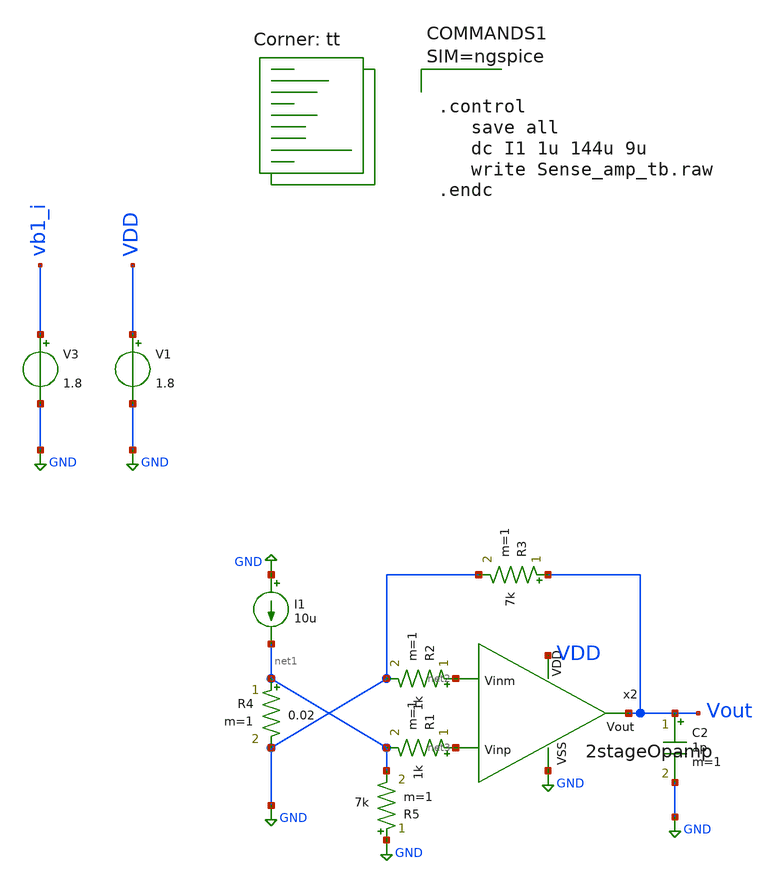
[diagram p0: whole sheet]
** sch_path: xschem/test/xschem/untitled-2.sch
**.subckt untitled-2
I1 GND net1 10u
V1 VDD GND 1.8
V3 vb1_i GND 1.8
x2 VDD net2 net3 Vout GND 2stageOpamp
R4 net1 GND 0.02 m=1
C2 Vout GND 1p m=1
R1 net3 net1 1k m=1
R2 net2 GND 1k m=1
R3 Vout GND 7k m=1
R5 GND net1 7k m=1
**** begin user architecture code
.lib $::SKYWATER_MODELS/sky130.lib.spice tt



.control
   save all
   dc I1 1u 144u 9u
   write Sense_amp_tb.raw
.endc



**** end user architecture code
**.ends

* expanding   symbol:  amplifiers/dec24/2stageOpamp.sym # of pins=5
** sym_path: amplifiers/dec24/2stageOpamp.sym
** sch_path: amplifiers/dec24/2stageOpamp.sch
.subckt 2stageOpamp VDD Vinm Vinp Vout VSS
*.ipin Vinm
*.ipin Vinp
*.opin Vout
*.ipin VSS
*.ipin VDD
XM8 Vout net1 VSS VSS sky130_fd_pr__nfet_01v8 L=1 W=6 nf=1 ad='int((nf+1)/2) * W/nf * 0.29' as='int((nf+2)/2) * W/nf * 0.29'
+ pd='2*int((nf+1)/2) * (W/nf + 0.29)' ps='2*int((nf+2)/2) * (W/nf + 0.29)' nrd='0.29 / W' nrs='0.29 / W'
+ sa=0 sb=0 sd=0 mult=8 m=8
XM2 Vout Vb1 VDD VDD sky130_fd_pr__pfet_01v8_lvt L=1 W=9 nf=1 ad='int((nf+1)/2) * W/nf * 0.29' as='int((nf+2)/2) * W/nf * 0.29'
+ pd='2*int((nf+1)/2) * (W/nf + 0.29)' ps='2*int((nf+2)/2) * (W/nf + 0.29)' nrd='0.29 / W' nrs='0.29 / W'
+ sa=0 sb=0 sd=0 mult=3 m=3
XM5 net5 Vb3 net6 VSS sky130_fd_pr__nfet_01v8 L=1 W=4 nf=1 ad='int((nf+1)/2) * W/nf * 0.29' as='int((nf+2)/2) * W/nf * 0.29'
+ pd='2*int((nf+1)/2) * (W/nf + 0.29)' ps='2*int((nf+2)/2) * (W/nf + 0.29)' nrd='0.29 / W' nrs='0.29 / W'
+ sa=0 sb=0 sd=0 mult=3 m=3
XM17 net1 Vb3 net7 VSS sky130_fd_pr__nfet_01v8 L=1 W=4 nf=1 ad='int((nf+1)/2) * W/nf * 0.29' as='int((nf+2)/2) * W/nf * 0.29'
+ pd='2*int((nf+1)/2) * (W/nf + 0.29)' ps='2*int((nf+2)/2) * (W/nf + 0.29)' nrd='0.29 / W' nrs='0.29 / W'
+ sa=0 sb=0 sd=0 mult=3 m=3
XM3 net6 net5 VSS VSS sky130_fd_pr__nfet_01v8 L=1 W=8 nf=1 ad='int((nf+1)/2) * W/nf * 0.29' as='int((nf+2)/2) * W/nf * 0.29'
+ pd='2*int((nf+1)/2) * (W/nf + 0.29)' ps='2*int((nf+2)/2) * (W/nf + 0.29)' nrd='0.29 / W' nrs='0.29 / W'
+ sa=0 sb=0 sd=0 mult=1 m=1
XM19 net7 net5 VSS VSS sky130_fd_pr__nfet_01v8 L=1 W=8 nf=1 ad='int((nf+1)/2) * W/nf * 0.29' as='int((nf+2)/2) * W/nf * 0.29'
+ pd='2*int((nf+1)/2) * (W/nf + 0.29)' ps='2*int((nf+2)/2) * (W/nf + 0.29)' nrd='0.29 / W' nrs='0.29 / W'
+ sa=0 sb=0 sd=0 mult=1 m=1
V1 Vb1 GND 1.1
V2 Vb2 GND 0.7
V3 Vb3 GND 0.9
XM11 net8 Vb1 VDD VDD sky130_fd_pr__pfet_01v8_lvt L=1 W=9 nf=1 ad='int((nf+1)/2) * W/nf * 0.29' as='int((nf+2)/2) * W/nf * 0.29'
+ pd='2*int((nf+1)/2) * (W/nf + 0.29)' ps='2*int((nf+2)/2) * (W/nf + 0.29)' nrd='0.29 / W' nrs='0.29 / W'
+ sa=0 sb=0 sd=0 mult=2 m=2
XM1 net6 Vinm net8 VDD sky130_fd_pr__pfet_01v8_lvt L=1 W=8 nf=1 ad='int((nf+1)/2) * W/nf * 0.29' as='int((nf+2)/2) * W/nf * 0.29'
+ pd='2*int((nf+1)/2) * (W/nf + 0.29)' ps='2*int((nf+2)/2) * (W/nf + 0.29)' nrd='0.29 / W' nrs='0.29 / W'
+ sa=0 sb=0 sd=0 mult=3 m=3
XM15 net7 Vinp net8 VDD sky130_fd_pr__pfet_01v8_lvt L=1 W=8 nf=1 ad='int((nf+1)/2) * W/nf * 0.29' as='int((nf+2)/2) * W/nf * 0.29'
+ pd='2*int((nf+1)/2) * (W/nf + 0.29)' ps='2*int((nf+2)/2) * (W/nf + 0.29)' nrd='0.29 / W' nrs='0.29 / W'
+ sa=0 sb=0 sd=0 mult=3 m=3
XM7 net3 Vb1 VDD VDD sky130_fd_pr__pfet_01v8_lvt L=1 W=9 nf=1 ad='int((nf+1)/2) * W/nf * 0.29' as='int((nf+2)/2) * W/nf * 0.29'
+ pd='2*int((nf+1)/2) * (W/nf + 0.29)' ps='2*int((nf+2)/2) * (W/nf + 0.29)' nrd='0.29 / W' nrs='0.29 / W'
+ sa=0 sb=0 sd=0 mult=1 m=1
XM21 net4 Vb1 VDD VDD sky130_fd_pr__pfet_01v8_lvt L=1 W=9 nf=1 ad='int((nf+1)/2) * W/nf * 0.29' as='int((nf+2)/2) * W/nf * 0.29'
+ pd='2*int((nf+1)/2) * (W/nf + 0.29)' ps='2*int((nf+2)/2) * (W/nf + 0.29)' nrd='0.29 / W' nrs='0.29 / W'
+ sa=0 sb=0 sd=0 mult=1 m=1
XM9 net5 Vb2 net3 VDD sky130_fd_pr__pfet_01v8_lvt L=1 W=9 nf=1 ad='int((nf+1)/2) * W/nf * 0.29' as='int((nf+2)/2) * W/nf * 0.29'
+ pd='2*int((nf+1)/2) * (W/nf + 0.29)' ps='2*int((nf+2)/2) * (W/nf + 0.29)' nrd='0.29 / W' nrs='0.29 / W'
+ sa=0 sb=0 sd=0 mult=1 m=1
XM23 net1 Vb2 net4 VDD sky130_fd_pr__pfet_01v8_lvt L=1 W=9 nf=1 ad='int((nf+1)/2) * W/nf * 0.29' as='int((nf+2)/2) * W/nf * 0.29'
+ pd='2*int((nf+1)/2) * (W/nf + 0.29)' ps='2*int((nf+2)/2) * (W/nf + 0.29)' nrd='0.29 / W' nrs='0.29 / W'
+ sa=0 sb=0 sd=0 mult=1 m=1
XC4 net2 Vout sky130_fd_pr__cap_mim_m3_2 W=7 L=7 MF=4 m=4
R4 net1 net2 7k m=1
.ends

.GLOBAL GND
.end
